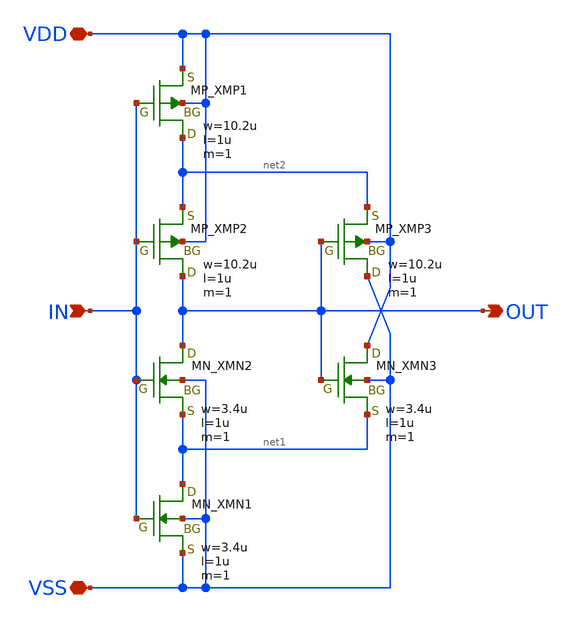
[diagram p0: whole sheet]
** sch_path: member_project/imager/YuMaehashi/design/schmitt_trigger.sch
**.subckt schmitt_trigger OUT IN VDD VSS
*.opin OUT
*.ipin IN
*.iopin VDD
*.iopin VSS
XXMN1 net1 IN VSS VSS NMOS w=3.4u l=1u nrd=0 nrs=0 m=1
XXMN2 OUT IN net1 VSS NMOS w=3.4u l=1u nrd=0 nrs=0 m=1
XXMP2 OUT IN net2 VDD PMOS w=10.2u l=1u nrd=0 nrs=0 m=1
XXMP1 net2 IN VDD VDD PMOS w=10.2u l=1u nrd=0 nrs=0 m=1
XXMP3 VSS OUT net2 VDD PMOS w=10.2u l=1u nrd=0 nrs=0 m=1
XXMN3 VDD OUT net1 VSS NMOS w=3.4u l=1u nrd=0 nrs=0 m=1
**.ends
.end
